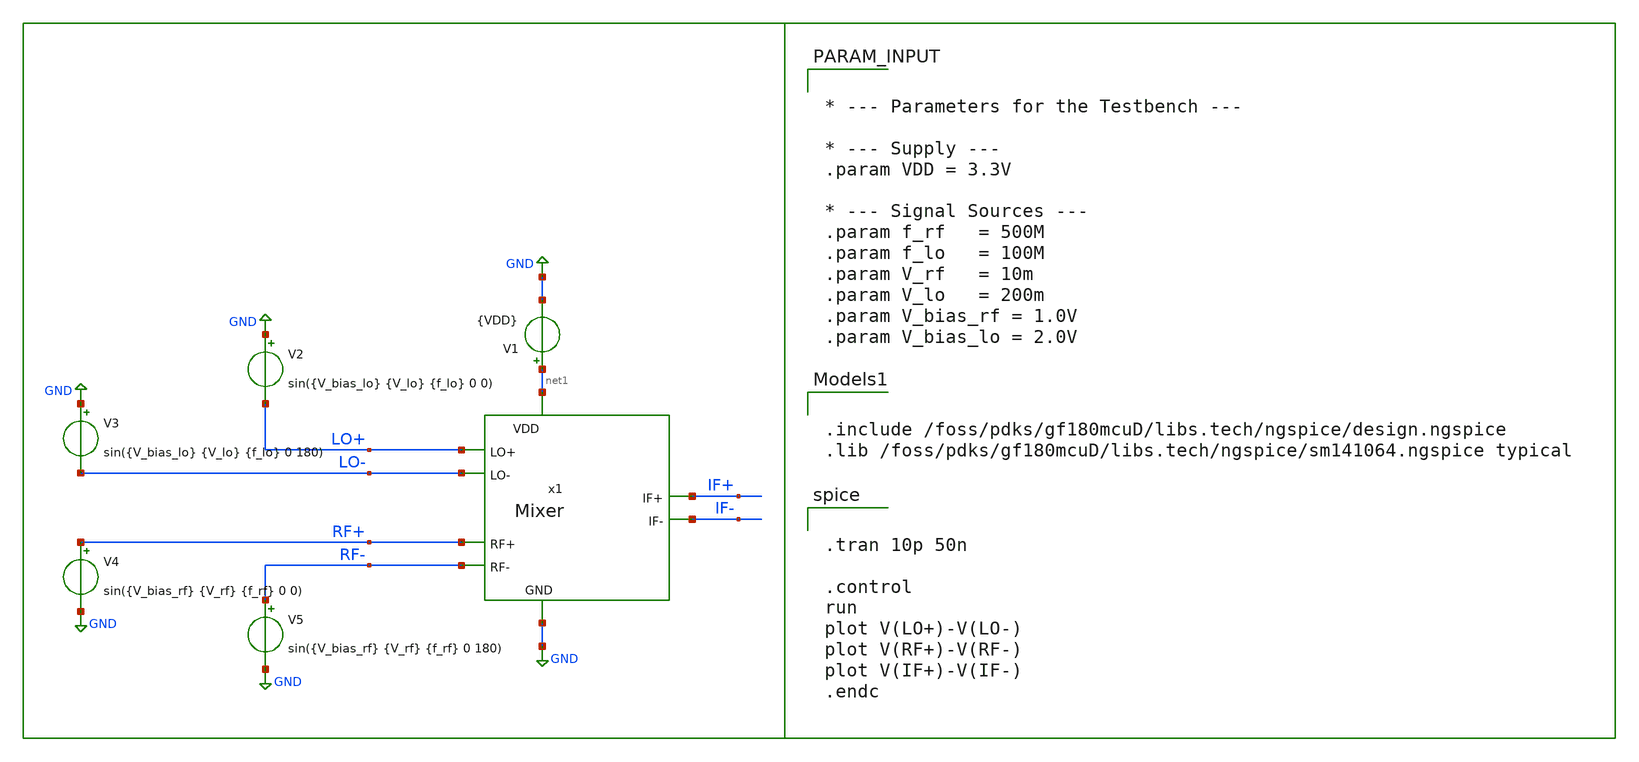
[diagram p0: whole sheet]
** sch_path: Project/1-on-chip/schematic/Mixer/tb_Mixer.sch
**.subckt tb_Mixer
x1 net1 GND LO+ LO- RF+ RF- IF+ IF- Mixer
V1 net1 GND {VDD}
V2 GND LO+ sin({V_bias_lo} {V_lo} {f_lo} 0 0)
V3 GND LO- sin({V_bias_lo} {V_lo} {f_lo} 0 180)
V4 RF+ GND sin({V_bias_rf} {V_rf} {f_rf} 0 0)
V5 RF- GND sin({V_bias_rf} {V_rf} {f_rf} 0 180)
**** begin user architecture code


.tran 10p 50n

.control
run
plot V(LO+)-V(LO-)
plot V(RF+)-V(RF-)
plot V(IF+)-V(IF-)
.endc



.include /foss/pdks/gf180mcuD/libs.tech/ngspice/design.ngspice
.lib /foss/pdks/gf180mcuD/libs.tech/ngspice/sm141064.ngspice typical



* --- Parameters for the Testbench ---

* --- Supply ---
.param VDD = 3.3V

* --- Signal Sources ---
.param f_rf   = 500M
.param f_lo   = 100M
.param V_rf   = 10m
.param V_lo   = 200m
.param V_bias_rf = 1.0V
.param V_bias_lo = 2.0V


**** end user architecture code
**.ends

* expanding   symbol:  Mixer.sym # of pins=8
** sym_path: Project/1-on-chip/schematic/Mixer/Mixer.sym
** sch_path: Project/1-on-chip/schematic/Mixer/Mixer.sch
.subckt Mixer VDD GND LO+ LO- RF+ RF- IF+ IF-
*.ipin GND
*.ipin RF+
*.ipin RF-
*.ipin VDD
*.ipin LO+
*.ipin LO-
*.opin IF-
*.opin IF+
XM8 net1 net1 GND GND nfet_03v3 L={L_min} W={W_bias_ref} nf=1 ad='int((nf+1)/2) * W/nf * 0.18u' as='int((nf+2)/2) * W/nf * 0.18u'
+ pd='2*int((nf+1)/2) * (W/nf + 0.18u)' ps='2*int((nf+2)/2) * (W/nf + 0.18u)' nrd='0.18u / W' nrs='0.18u / W'
+ sa=0 sb=0 sd=0 m=1
XM1 net2 net1 GND GND nfet_03v3 L={L_min} W={W_bias_out} nf=1 ad='int((nf+1)/2) * W/nf * 0.18u' as='int((nf+2)/2) * W/nf * 0.18u'
+ pd='2*int((nf+1)/2) * (W/nf + 0.18u)' ps='2*int((nf+2)/2) * (W/nf + 0.18u)' nrd='0.18u / W' nrs='0.18u / W'
+ sa=0 sb=0 sd=0 m=1
XM3 net8 net4 net2 GND nfet_03v3 L={L_min} W={W_rf} nf=1 ad='int((nf+1)/2) * W/nf * 0.18u' as='int((nf+2)/2) * W/nf * 0.18u'
+ pd='2*int((nf+1)/2) * (W/nf + 0.18u)' ps='2*int((nf+2)/2) * (W/nf + 0.18u)' nrd='0.18u / W' nrs='0.18u / W'
+ sa=0 sb=0 sd=0 m=1
XM2 net7 net6 net2 GND nfet_03v3 L={L_min} W={W_rf} nf=1 ad='int((nf+1)/2) * W/nf * 0.18u' as='int((nf+2)/2) * W/nf * 0.18u'
+ pd='2*int((nf+1)/2) * (W/nf + 0.18u)' ps='2*int((nf+2)/2) * (W/nf + 0.18u)' nrd='0.18u / W' nrs='0.18u / W'
+ sa=0 sb=0 sd=0 m=1
CGS2 net4 net2 {C_gate} m=1
LG2 net3 RF- {L_gate} m=1
CGS1 net6 net2 {C_gate} m=1
LG1 RF+ net5 {L_gate} m=1
RG1 net5 net6 {R_gate} m=1
RG2 net4 net3 {R_gate} m=1
XM7 IF- LO+ net8 GND nfet_03v3 L={L_min} W={W_sw} nf=1 ad='int((nf+1)/2) * W/nf * 0.18u' as='int((nf+2)/2) * W/nf * 0.18u'
+ pd='2*int((nf+1)/2) * (W/nf + 0.18u)' ps='2*int((nf+2)/2) * (W/nf + 0.18u)' nrd='0.18u / W' nrs='0.18u / W'
+ sa=0 sb=0 sd=0 m=1
XM6 IF+ LO- net8 GND nfet_03v3 L={L_min} W={W_sw} nf=1 ad='int((nf+1)/2) * W/nf * 0.18u' as='int((nf+2)/2) * W/nf * 0.18u'
+ pd='2*int((nf+1)/2) * (W/nf + 0.18u)' ps='2*int((nf+2)/2) * (W/nf + 0.18u)' nrd='0.18u / W' nrs='0.18u / W'
+ sa=0 sb=0 sd=0 m=1
XM5 IF- LO- net7 GND nfet_03v3 L={L_min} W={W_sw} nf=1 ad='int((nf+1)/2) * W/nf * 0.18u' as='int((nf+2)/2) * W/nf * 0.18u'
+ pd='2*int((nf+1)/2) * (W/nf + 0.18u)' ps='2*int((nf+2)/2) * (W/nf + 0.18u)' nrd='0.18u / W' nrs='0.18u / W'
+ sa=0 sb=0 sd=0 m=1
XM4 IF+ LO+ net7 GND nfet_03v3 L={L_min} W={W_sw} nf=1 ad='int((nf+1)/2) * W/nf * 0.18u' as='int((nf+2)/2) * W/nf * 0.18u'
+ pd='2*int((nf+1)/2) * (W/nf + 0.18u)' ps='2*int((nf+2)/2) * (W/nf + 0.18u)' nrd='0.18u / W' nrs='0.18u / W'
+ sa=0 sb=0 sd=0 m=1
RD2 VDD IF- {R_load} m=1
RD1 VDD IF+ {R_load} m=1
Rbias VDD net1 {R_bias} m=1
**** begin user architecture code


* --- Technology ---
.param L_min = 0.28u

* --- Transistor W/L Ratios ---
.param WL_rf_ratio       = 54
.param WL_sw_ratio       = 27
.param WL_bias_ref_ratio = 5
.param WL_bias_out_ratio = 50

* --- Resistors ---
.param R_load = 450
.param R_bias = 10k

* --- Impedance Matching for 100MHz ---
.param R_gate = 50
.param C_gate = 12.7p
.param L_gate = 200n

* --- Calculated Transistor Widths ---
.param W_rf       = {WL_rf_ratio * L_min}
.param W_sw       = {WL_sw_ratio * L_min}
.param W_bias_ref = {WL_bias_ref_ratio * L_min}
.param W_bias_out = {WL_bias_out_ratio * L_min}



**** end user architecture code
I0 net9 net10 2m
.ends

.GLOBAL GND
.end
